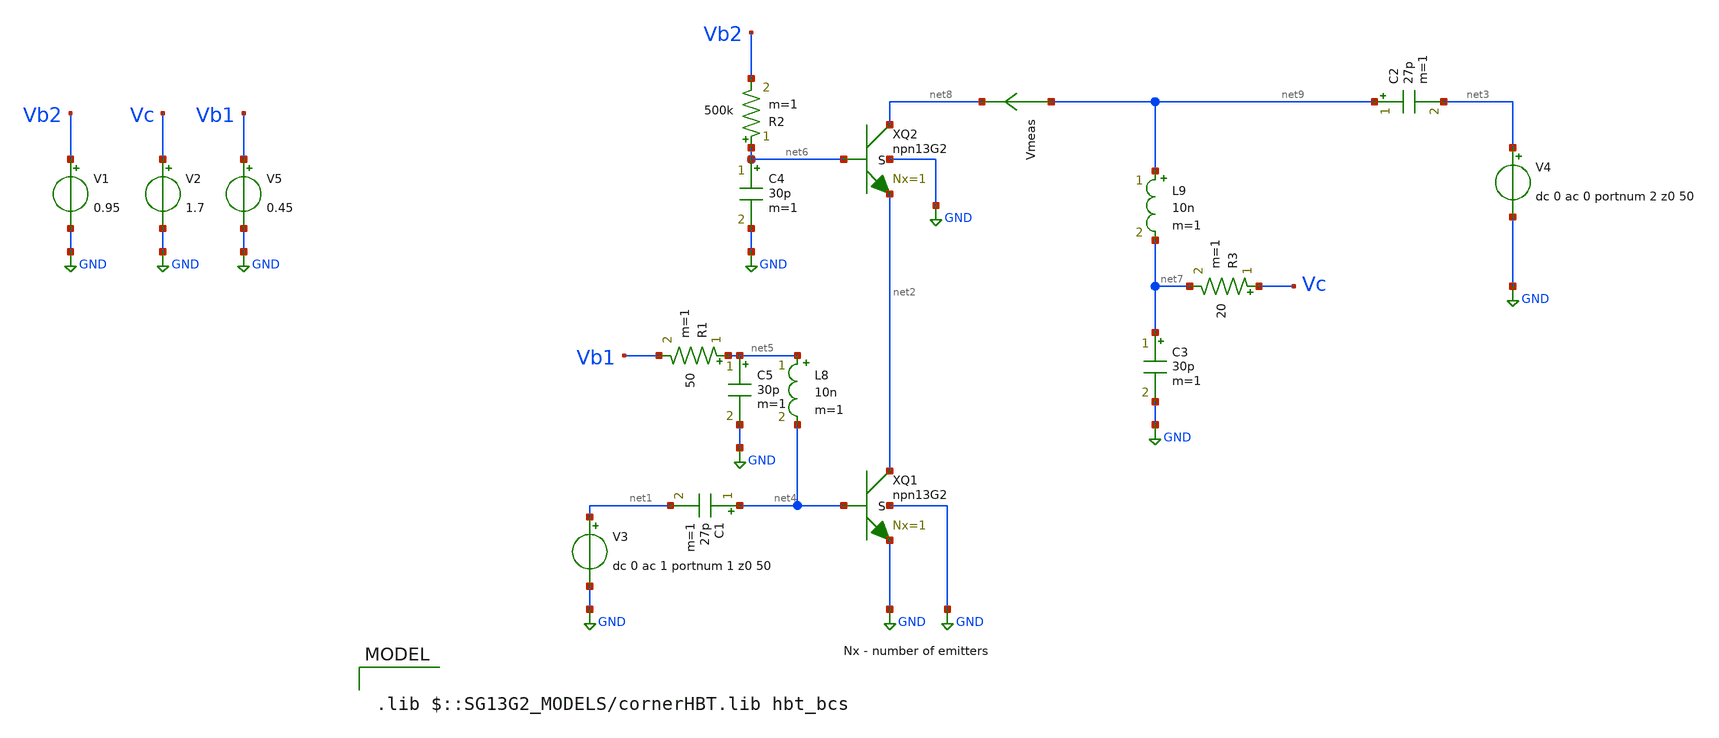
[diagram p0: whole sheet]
** sch_path: ihp-sg13g2/libs.tech/xschem/sg13g2_tests/sp_hbt_13g2_cascode.sch
* Copyright 2023 IHP PDK Authors
**.subckt sp_hbt_13g2_cascode
V4 net3 GND dc 0 ac 0 portnum 2 z0 50
XQ1 net2 net4 GND GND npn13G2 Nx=1
V3 net1 GND dc 0 ac 1 portnum 1 z0 50
V1 Vb2 GND 0.95
V2 Vc GND 1.7
C1 net4 net1 27p m=1
C2 net9 net3 27p m=1
L8 net5 net4 10n m=1
L9 net9 net7 10n m=1
V5 Vb1 GND 0.45
R1 net5 Vb1 50 m=1
XQ2 net8 net6 net2 GND npn13G2 Nx=1
R2 net6 Vb2 500k m=1
R3 Vc net7 20 m=1
C3 net7 GND 30p m=1
C4 net6 GND 30p m=1
C5 net5 GND 30p m=1
Vmeas net9 net8 0
.save i(vmeas)
**** begin user architecture code

.lib $::SG13G2_MODELS/cornerHBT.lib hbt_bcs



.param Rbase=50
.control
save all
sp dec 500 1e8 1e12
*meas ac z11 FIND z_1_1 AT=1e10
let phiz = ph(z_1_1)
*meas ac pz11 FIND phiz AT=1e10
*let X = z11*cos(pz11)
*let Y = z11*sin(pz11)
*print X, Y
print I(Vmeas)
write sp_hbt_13g2_lna.raw
.endc


**** end user architecture code
**.ends
.GLOBAL GND
.end
